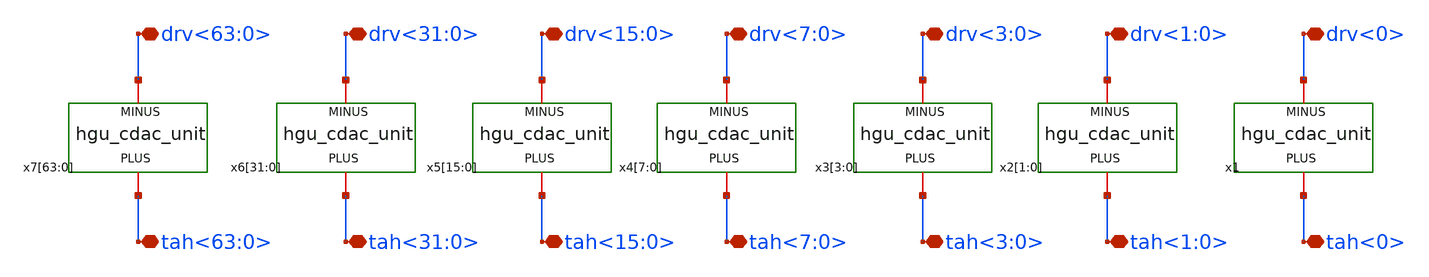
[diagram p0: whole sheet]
** sch_path: hgu/xschem/hgu_cdac_8bit_array.sch
**.subckt hgu_cdac_8bit_array drv<0> drv<1:0> drv<3:0> drv<7:0> drv<15:0> drv<31:0> drv<63:0> tah<0>
*+ tah<1:0> tah<3:0> tah<7:0> tah<15:0> tah<31:0> tah<63:0>
*.iopin drv<0>
*.iopin drv<1:0>
*.iopin drv<3:0>
*.iopin drv<7:0>
*.iopin drv<15:0>
*.iopin drv<31:0>
*.iopin drv<63:0>
*.iopin tah<0>
*.iopin tah<1:0>
*.iopin tah<3:0>
*.iopin tah<7:0>
*.iopin tah<15:0>
*.iopin tah<31:0>
*.iopin tah<63:0>
x1 tah<0> drv<0> hgu_cdac_unit csize=1
x2[1] tah<1:0> drv<1:0> hgu_cdac_unit csize=1
x2[0] tah<1:0> drv<1:0> hgu_cdac_unit csize=1
x3[3] tah<3:0> drv<3:0> hgu_cdac_unit csize=1
x3[2] tah<3:0> drv<3:0> hgu_cdac_unit csize=1
x3[1] tah<3:0> drv<3:0> hgu_cdac_unit csize=1
x3[0] tah<3:0> drv<3:0> hgu_cdac_unit csize=1
x4[7] tah<7:0> drv<7:0> hgu_cdac_unit csize=1
x4[6] tah<7:0> drv<7:0> hgu_cdac_unit csize=1
x4[5] tah<7:0> drv<7:0> hgu_cdac_unit csize=1
x4[4] tah<7:0> drv<7:0> hgu_cdac_unit csize=1
x4[3] tah<7:0> drv<7:0> hgu_cdac_unit csize=1
x4[2] tah<7:0> drv<7:0> hgu_cdac_unit csize=1
x4[1] tah<7:0> drv<7:0> hgu_cdac_unit csize=1
x4[0] tah<7:0> drv<7:0> hgu_cdac_unit csize=1
x5[15] tah<15:0> drv<15:0> hgu_cdac_unit csize=1
x5[14] tah<15:0> drv<15:0> hgu_cdac_unit csize=1
x5[13] tah<15:0> drv<15:0> hgu_cdac_unit csize=1
x5[12] tah<15:0> drv<15:0> hgu_cdac_unit csize=1
x5[11] tah<15:0> drv<15:0> hgu_cdac_unit csize=1
x5[10] tah<15:0> drv<15:0> hgu_cdac_unit csize=1
x5[9] tah<15:0> drv<15:0> hgu_cdac_unit csize=1
x5[8] tah<15:0> drv<15:0> hgu_cdac_unit csize=1
x5[7] tah<15:0> drv<15:0> hgu_cdac_unit csize=1
x5[6] tah<15:0> drv<15:0> hgu_cdac_unit csize=1
x5[5] tah<15:0> drv<15:0> hgu_cdac_unit csize=1
x5[4] tah<15:0> drv<15:0> hgu_cdac_unit csize=1
x5[3] tah<15:0> drv<15:0> hgu_cdac_unit csize=1
x5[2] tah<15:0> drv<15:0> hgu_cdac_unit csize=1
x5[1] tah<15:0> drv<15:0> hgu_cdac_unit csize=1
x5[0] tah<15:0> drv<15:0> hgu_cdac_unit csize=1
x6[31] tah<31:0> drv<31:0> hgu_cdac_unit csize=1
x6[30] tah<31:0> drv<31:0> hgu_cdac_unit csize=1
x6[29] tah<31:0> drv<31:0> hgu_cdac_unit csize=1
x6[28] tah<31:0> drv<31:0> hgu_cdac_unit csize=1
x6[27] tah<31:0> drv<31:0> hgu_cdac_unit csize=1
x6[26] tah<31:0> drv<31:0> hgu_cdac_unit csize=1
x6[25] tah<31:0> drv<31:0> hgu_cdac_unit csize=1
x6[24] tah<31:0> drv<31:0> hgu_cdac_unit csize=1
x6[23] tah<31:0> drv<31:0> hgu_cdac_unit csize=1
x6[22] tah<31:0> drv<31:0> hgu_cdac_unit csize=1
x6[21] tah<31:0> drv<31:0> hgu_cdac_unit csize=1
x6[20] tah<31:0> drv<31:0> hgu_cdac_unit csize=1
x6[19] tah<31:0> drv<31:0> hgu_cdac_unit csize=1
x6[18] tah<31:0> drv<31:0> hgu_cdac_unit csize=1
x6[17] tah<31:0> drv<31:0> hgu_cdac_unit csize=1
x6[16] tah<31:0> drv<31:0> hgu_cdac_unit csize=1
x6[15] tah<31:0> drv<31:0> hgu_cdac_unit csize=1
x6[14] tah<31:0> drv<31:0> hgu_cdac_unit csize=1
x6[13] tah<31:0> drv<31:0> hgu_cdac_unit csize=1
x6[12] tah<31:0> drv<31:0> hgu_cdac_unit csize=1
x6[11] tah<31:0> drv<31:0> hgu_cdac_unit csize=1
x6[10] tah<31:0> drv<31:0> hgu_cdac_unit csize=1
x6[9] tah<31:0> drv<31:0> hgu_cdac_unit csize=1
x6[8] tah<31:0> drv<31:0> hgu_cdac_unit csize=1
x6[7] tah<31:0> drv<31:0> hgu_cdac_unit csize=1
x6[6] tah<31:0> drv<31:0> hgu_cdac_unit csize=1
x6[5] tah<31:0> drv<31:0> hgu_cdac_unit csize=1
x6[4] tah<31:0> drv<31:0> hgu_cdac_unit csize=1
x6[3] tah<31:0> drv<31:0> hgu_cdac_unit csize=1
x6[2] tah<31:0> drv<31:0> hgu_cdac_unit csize=1
x6[1] tah<31:0> drv<31:0> hgu_cdac_unit csize=1
x6[0] tah<31:0> drv<31:0> hgu_cdac_unit csize=1
x7[63] tah<63:0> drv<63:0> hgu_cdac_unit csize=1
x7[62] tah<63:0> drv<63:0> hgu_cdac_unit csize=1
x7[61] tah<63:0> drv<63:0> hgu_cdac_unit csize=1
x7[60] tah<63:0> drv<63:0> hgu_cdac_unit csize=1
x7[59] tah<63:0> drv<63:0> hgu_cdac_unit csize=1
x7[58] tah<63:0> drv<63:0> hgu_cdac_unit csize=1
x7[57] tah<63:0> drv<63:0> hgu_cdac_unit csize=1
x7[56] tah<63:0> drv<63:0> hgu_cdac_unit csize=1
x7[55] tah<63:0> drv<63:0> hgu_cdac_unit csize=1
x7[54] tah<63:0> drv<63:0> hgu_cdac_unit csize=1
x7[53] tah<63:0> drv<63:0> hgu_cdac_unit csize=1
x7[52] tah<63:0> drv<63:0> hgu_cdac_unit csize=1
x7[51] tah<63:0> drv<63:0> hgu_cdac_unit csize=1
x7[50] tah<63:0> drv<63:0> hgu_cdac_unit csize=1
x7[49] tah<63:0> drv<63:0> hgu_cdac_unit csize=1
x7[48] tah<63:0> drv<63:0> hgu_cdac_unit csize=1
x7[47] tah<63:0> drv<63:0> hgu_cdac_unit csize=1
x7[46] tah<63:0> drv<63:0> hgu_cdac_unit csize=1
x7[45] tah<63:0> drv<63:0> hgu_cdac_unit csize=1
x7[44] tah<63:0> drv<63:0> hgu_cdac_unit csize=1
x7[43] tah<63:0> drv<63:0> hgu_cdac_unit csize=1
x7[42] tah<63:0> drv<63:0> hgu_cdac_unit csize=1
x7[41] tah<63:0> drv<63:0> hgu_cdac_unit csize=1
x7[40] tah<63:0> drv<63:0> hgu_cdac_unit csize=1
x7[39] tah<63:0> drv<63:0> hgu_cdac_unit csize=1
x7[38] tah<63:0> drv<63:0> hgu_cdac_unit csize=1
x7[37] tah<63:0> drv<63:0> hgu_cdac_unit csize=1
x7[36] tah<63:0> drv<63:0> hgu_cdac_unit csize=1
x7[35] tah<63:0> drv<63:0> hgu_cdac_unit csize=1
x7[34] tah<63:0> drv<63:0> hgu_cdac_unit csize=1
x7[33] tah<63:0> drv<63:0> hgu_cdac_unit csize=1
x7[32] tah<63:0> drv<63:0> hgu_cdac_unit csize=1
x7[31] tah<63:0> drv<63:0> hgu_cdac_unit csize=1
x7[30] tah<63:0> drv<63:0> hgu_cdac_unit csize=1
x7[29] tah<63:0> drv<63:0> hgu_cdac_unit csize=1
x7[28] tah<63:0> drv<63:0> hgu_cdac_unit csize=1
x7[27] tah<63:0> drv<63:0> hgu_cdac_unit csize=1
x7[26] tah<63:0> drv<63:0> hgu_cdac_unit csize=1
x7[25] tah<63:0> drv<63:0> hgu_cdac_unit csize=1
x7[24] tah<63:0> drv<63:0> hgu_cdac_unit csize=1
x7[23] tah<63:0> drv<63:0> hgu_cdac_unit csize=1
x7[22] tah<63:0> drv<63:0> hgu_cdac_unit csize=1
x7[21] tah<63:0> drv<63:0> hgu_cdac_unit csize=1
x7[20] tah<63:0> drv<63:0> hgu_cdac_unit csize=1
x7[19] tah<63:0> drv<63:0> hgu_cdac_unit csize=1
x7[18] tah<63:0> drv<63:0> hgu_cdac_unit csize=1
x7[17] tah<63:0> drv<63:0> hgu_cdac_unit csize=1
x7[16] tah<63:0> drv<63:0> hgu_cdac_unit csize=1
x7[15] tah<63:0> drv<63:0> hgu_cdac_unit csize=1
x7[14] tah<63:0> drv<63:0> hgu_cdac_unit csize=1
x7[13] tah<63:0> drv<63:0> hgu_cdac_unit csize=1
x7[12] tah<63:0> drv<63:0> hgu_cdac_unit csize=1
x7[11] tah<63:0> drv<63:0> hgu_cdac_unit csize=1
x7[10] tah<63:0> drv<63:0> hgu_cdac_unit csize=1
x7[9] tah<63:0> drv<63:0> hgu_cdac_unit csize=1
x7[8] tah<63:0> drv<63:0> hgu_cdac_unit csize=1
x7[7] tah<63:0> drv<63:0> hgu_cdac_unit csize=1
x7[6] tah<63:0> drv<63:0> hgu_cdac_unit csize=1
x7[5] tah<63:0> drv<63:0> hgu_cdac_unit csize=1
x7[4] tah<63:0> drv<63:0> hgu_cdac_unit csize=1
x7[3] tah<63:0> drv<63:0> hgu_cdac_unit csize=1
x7[2] tah<63:0> drv<63:0> hgu_cdac_unit csize=1
x7[1] tah<63:0> drv<63:0> hgu_cdac_unit csize=1
x7[0] tah<63:0> drv<63:0> hgu_cdac_unit csize=1
**.ends

* expanding   symbol:  hgu_cdac_unit.sym # of pins=2
** sym_path: hgu/xschem/hgu_cdac_unit.sym
** sch_path: hgu/xschem/hgu_cdac_unit.sch
.subckt hgu_cdac_unit PLUS MINUS  csize=csize
*.iopin PLUS
*.iopin MINUS
C1 PLUS MINUS 9f m=csize
.ends

.end
